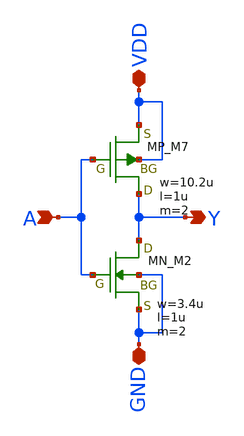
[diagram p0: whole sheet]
** sch_path: libs.tech/xschem/TR-1um_stdcell/INV_X2.sch
**.subckt INV_X2 A Y GND VDD
*.ipin A
*.opin Y
*.iopin GND
*.iopin VDD
XM7 Y A VDD VDD PMOS w=10.2u l=1u nrd=0 nrs=0 m=2
XM2 Y A GND GND NMOS w=3.4u l=1u nrd=0 nrs=0 m=2
**.ends
.end
